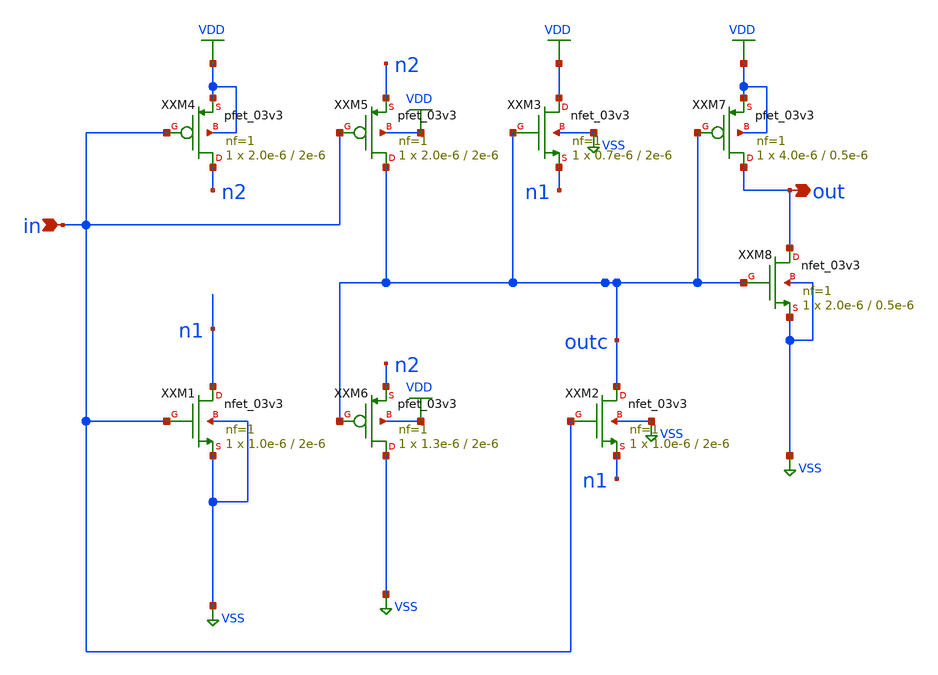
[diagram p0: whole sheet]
** sch_path: design/analog/schmitt_trigger/schmitt_trigger.sch
**.subckt schmitt_trigger in out
*.ipin in
*.opin out
XXM4 n2 in VDD VDD pfet_03v3 L=2e-6 W=2.0e-6 nf=1 ad='int((nf+1)/2) * W/nf * 0.18u' as='int((nf+2)/2) * W/nf * 0.18u'
+ pd='2*int((nf+1)/2) * (W/nf + 0.18u)' ps='2*int((nf+2)/2) * (W/nf + 0.18u)' nrd='0.18u / W' nrs='0.18u / W'
+ sa=0 sb=0 sd=0 m=1
XXM5 outc in n2 VDD pfet_03v3 L=2e-6 W=2.0e-6 nf=1 ad='int((nf+1)/2) * W/nf * 0.18u' as='int((nf+2)/2) * W/nf * 0.18u'
+ pd='2*int((nf+1)/2) * (W/nf + 0.18u)' ps='2*int((nf+2)/2) * (W/nf + 0.18u)' nrd='0.18u / W' nrs='0.18u / W'
+ sa=0 sb=0 sd=0 m=1
XXM6 VSS outc n2 VDD pfet_03v3 L=2e-6 W=1.3e-6 nf=1 ad='int((nf+1)/2) * W/nf * 0.18u' as='int((nf+2)/2) * W/nf * 0.18u'
+ pd='2*int((nf+1)/2) * (W/nf + 0.18u)' ps='2*int((nf+2)/2) * (W/nf + 0.18u)' nrd='0.18u / W' nrs='0.18u / W'
+ sa=0 sb=0 sd=0 m=1
XXM1 n1 in VSS VSS nfet_03v3 L=2e-6 W=1.0e-6 nf=1 ad='int((nf+1)/2) * W/nf * 0.18u' as='int((nf+2)/2) * W/nf * 0.18u'
+ pd='2*int((nf+1)/2) * (W/nf + 0.18u)' ps='2*int((nf+2)/2) * (W/nf + 0.18u)' nrd='0.18u / W' nrs='0.18u / W'
+ sa=0 sb=0 sd=0 m=1
XXM2 outc in n1 VSS nfet_03v3 L=2e-6 W=1.0e-6 nf=1 ad='int((nf+1)/2) * W/nf * 0.18u' as='int((nf+2)/2) * W/nf * 0.18u'
+ pd='2*int((nf+1)/2) * (W/nf + 0.18u)' ps='2*int((nf+2)/2) * (W/nf + 0.18u)' nrd='0.18u / W' nrs='0.18u / W'
+ sa=0 sb=0 sd=0 m=1
XXM3 VDD outc n1 VSS nfet_03v3 L=2e-6 W=0.7e-6 nf=1 ad='int((nf+1)/2) * W/nf * 0.18u' as='int((nf+2)/2) * W/nf * 0.18u'
+ pd='2*int((nf+1)/2) * (W/nf + 0.18u)' ps='2*int((nf+2)/2) * (W/nf + 0.18u)' nrd='0.18u / W' nrs='0.18u / W'
+ sa=0 sb=0 sd=0 m=1
XXM7 out outc VDD VDD pfet_03v3 L=0.5e-6 W=4.0e-6 nf=1 ad='int((nf+1)/2) * W/nf * 0.18u' as='int((nf+2)/2) * W/nf * 0.18u'
+ pd='2*int((nf+1)/2) * (W/nf + 0.18u)' ps='2*int((nf+2)/2) * (W/nf + 0.18u)' nrd='0.18u / W' nrs='0.18u / W'
+ sa=0 sb=0 sd=0 m=1
XXM8 out outc VSS VSS nfet_03v3 L=0.5e-6 W=2.0e-6 nf=1 ad='int((nf+1)/2) * W/nf * 0.18u' as='int((nf+2)/2) * W/nf * 0.18u'
+ pd='2*int((nf+1)/2) * (W/nf + 0.18u)' ps='2*int((nf+2)/2) * (W/nf + 0.18u)' nrd='0.18u / W' nrs='0.18u / W'
+ sa=0 sb=0 sd=0 m=1
**.ends
.GLOBAL VDD
.GLOBAL VSS
.end
